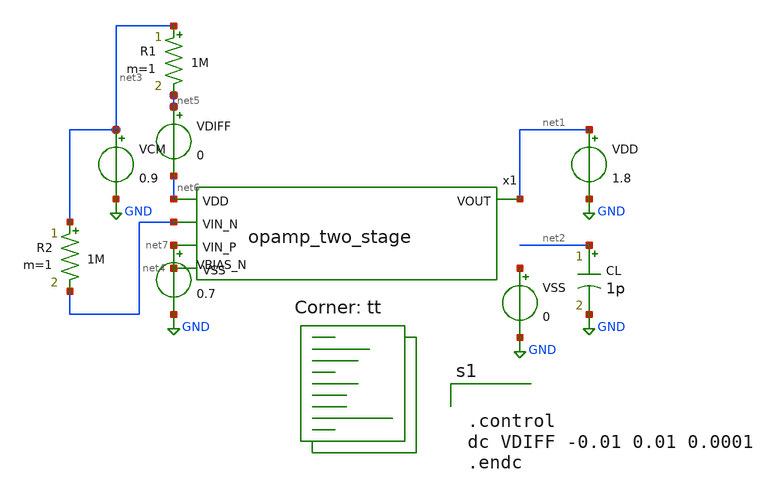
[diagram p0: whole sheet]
** sch_path: analog/build/schematic/opamp_two_stage_tb.sch
**.subckt opamp_two_stage_tb
x1 net6 net1 net4 net7 net8 opamp_two_stage
VDD net1 GND 1.8
VCM net3 GND 0.9
VBIAS_N net7 GND 0.7
CL net2 GND 1p m=1
VSS net9 GND 0
R1 net3 net5 1M m=1
R2 net3 net4 1M m=1
VDIFF net5 net6 0
**** begin user architecture code
.lib $::SKYWATER_MODELS/sky130.lib.spice tt


.control
dc VDIFF -0.01 0.01 0.0001
.endc


**** end user architecture code
**.ends

* expanding   symbol:  opamp_two_stage.sym # of pins=5
** sym_path: analog/build/schematic/opamp_two_stage.sym
** sch_path: analog/build/schematic/opamp_two_stage.sch
.subckt opamp_two_stage VDD VOUT VIN_N VIN_P VSS
*.ipin VIN_N
*.ipin VIN_P
*.opin VOUT
*.ipin VDD
*.ipin VSS
XM1 net3 VIN_N net1 VSS sky130_fd_pr__nfet_01v8 L=1 W=10 nf=1 ad='int((nf+1)/2) * W/nf * 0.29' as='int((nf+2)/2) * W/nf * 0.29'
+ pd='2*int((nf+1)/2) * (W/nf + 0.29)' ps='2*int((nf+2)/2) * (W/nf + 0.29)' nrd='0.29 / W' nrs='0.29 / W'
+ sa=0 sb=0 sd=0 mult=1 m=1
XM2 net2 VIN_P net1 VSS sky130_fd_pr__nfet_01v8 L=1 W=10 nf=1 ad='int((nf+1)/2) * W/nf * 0.29' as='int((nf+2)/2) * W/nf * 0.29'
+ pd='2*int((nf+1)/2) * (W/nf + 0.29)' ps='2*int((nf+2)/2) * (W/nf + 0.29)' nrd='0.29 / W' nrs='0.29 / W'
+ sa=0 sb=0 sd=0 mult=1 m=1
XM3 net1 net5 VSS VSS sky130_fd_pr__nfet_01v8 L=2 W=10 nf=1 ad='int((nf+1)/2) * W/nf * 0.29' as='int((nf+2)/2) * W/nf * 0.29'
+ pd='2*int((nf+1)/2) * (W/nf + 0.29)' ps='2*int((nf+2)/2) * (W/nf + 0.29)' nrd='0.29 / W' nrs='0.29 / W'
+ sa=0 sb=0 sd=0 mult=1 m=1
XM4 net3 net2 VDD VDD sky130_fd_pr__pfet_01v8 L=1 W=20 nf=1 ad='int((nf+1)/2) * W/nf * 0.29' as='int((nf+2)/2) * W/nf * 0.29'
+ pd='2*int((nf+1)/2) * (W/nf + 0.29)' ps='2*int((nf+2)/2) * (W/nf + 0.29)' nrd='0.29 / W' nrs='0.29 / W'
+ sa=0 sb=0 sd=0 mult=1 m=1
XM5 net2 net2 VDD VDD sky130_fd_pr__pfet_01v8 L=1 W=20 nf=1 ad='int((nf+1)/2) * W/nf * 0.29' as='int((nf+2)/2) * W/nf * 0.29'
+ pd='2*int((nf+1)/2) * (W/nf + 0.29)' ps='2*int((nf+2)/2) * (W/nf + 0.29)' nrd='0.29 / W' nrs='0.29 / W'
+ sa=0 sb=0 sd=0 mult=1 m=1
XM7 VOUT net5 VSS VSS sky130_fd_pr__nfet_01v8 L=2 W=10 nf=1 ad='int((nf+1)/2) * W/nf * 0.29' as='int((nf+2)/2) * W/nf * 0.29'
+ pd='2*int((nf+1)/2) * (W/nf + 0.29)' ps='2*int((nf+2)/2) * (W/nf + 0.29)' nrd='0.29 / W' nrs='0.29 / W'
+ sa=0 sb=0 sd=0 mult=1 m=1
XM8 VOUT net3 VDD VDD sky130_fd_pr__pfet_01v8 L=1 W=20 nf=1 ad='int((nf+1)/2) * W/nf * 0.29' as='int((nf+2)/2) * W/nf * 0.29'
+ pd='2*int((nf+1)/2) * (W/nf + 0.29)' ps='2*int((nf+2)/2) * (W/nf + 0.29)' nrd='0.29 / W' nrs='0.29 / W'
+ sa=0 sb=0 sd=0 mult=1 m=1
C1 net3 net4 1p m=1
R1 VOUT net4 2k m=1
XM_bias net5 net5 VSS VSS sky130_fd_pr__nfet_01v8 L=2 W=10 nf=1 ad='int((nf+1)/2) * W/nf * 0.29' as='int((nf+2)/2) * W/nf * 0.29'
+ pd='2*int((nf+1)/2) * (W/nf + 0.29)' ps='2*int((nf+2)/2) * (W/nf + 0.29)' nrd='0.29 / W' nrs='0.29 / W'
+ sa=0 sb=0 sd=0 mult=1 m=1
R2 VDD net5 10k m=1
.ends

.GLOBAL GND
.end
